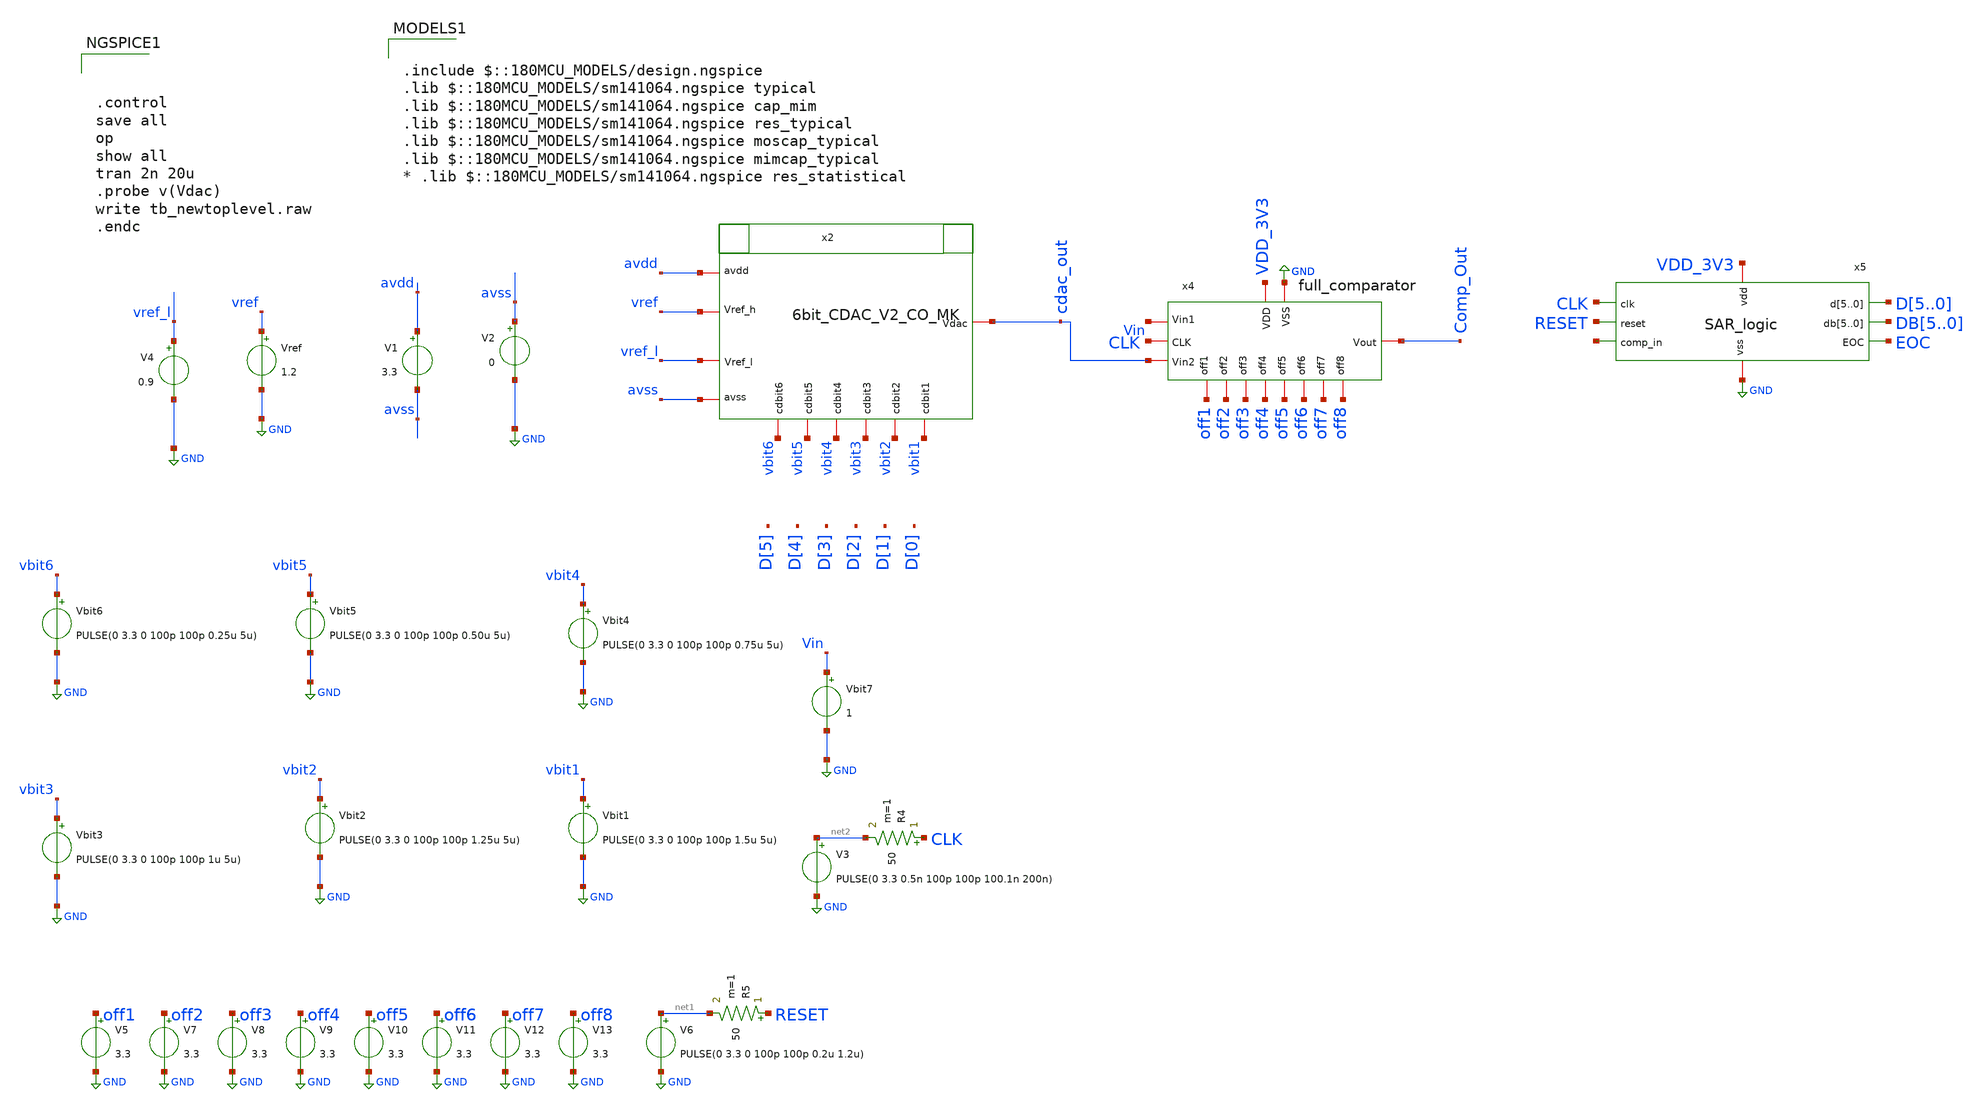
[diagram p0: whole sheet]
** sch_path: designs/full_ADC/tb_newtoplevel.sch
**.subckt tb_newtoplevel
V1 avdd avss 3.3
V2 avss GND 0
Vref vref GND 1.2
V5 off1 GND 3.3
V7 off2 GND 3.3
V8 off3 GND 3.3
V9 off4 GND 3.3
V10 off5 GND 3.3
V11 off6 GND 3.3
V12 off7 GND 3.3
V13 off8 GND 3.3
V6 net1 GND PULSE(0 3.3 0 100p 100p 0.2u 1.2u)
R5 RESET net1 50 m=1
x4 off1 VDD_3V3 GND off2 CLK off3 Vin off4 cdac_out off5 Comp_Out off6 off7 off8 full_comparator
x5 VDD_3V3 GND CLK RESET net3 D5 D4 D3 D2 D1 D0 DB5 DB4 DB3 DB2 DB1 DB0 EOC SAR_logic
Vbit7 Vin GND 1
V3 net2 GND PULSE(0 3.3 0.5n 100p 100p 100.1n 200n)
R4 CLK net2 50 m=1
x2 vref_l cdac_out avdd avss vref vbit6 vbit5 vbit3 vbit1 vbit2 vbit4 6bit_CDAC_V2_CO_MK
V4 vref_l GND 0.9
Vbit1 vbit1 GND PULSE(0 3.3 0 100p 100p 1.5u 5u)
Vbit2 vbit2 GND PULSE(0 3.3 0 100p 100p 1.25u 5u)
Vbit3 vbit3 GND PULSE(0 3.3 0 100p 100p 1u 5u)
Vbit4 vbit4 GND PULSE(0 3.3 0 100p 100p 0.75u 5u)
Vbit5 vbit5 GND PULSE(0 3.3 0 100p 100p 0.50u 5u)
Vbit6 vbit6 GND PULSE(0 3.3 0 100p 100p 0.25u 5u)
**** begin user architecture code



.control
save all
op
show all
tran 2n 20u
.probe v(Vdac)
write tb_newtoplevel.raw
.endc



.include $::180MCU_MODELS/design.ngspice
.lib $::180MCU_MODELS/sm141064.ngspice typical
.lib $::180MCU_MODELS/sm141064.ngspice cap_mim
.lib $::180MCU_MODELS/sm141064.ngspice res_typical
.lib $::180MCU_MODELS/sm141064.ngspice moscap_typical
.lib $::180MCU_MODELS/sm141064.ngspice mimcap_typical
* .lib $::180MCU_MODELS/sm141064.ngspice res_statistical

**** end user architecture code
**.ends
.GLOBAL GND
.end
